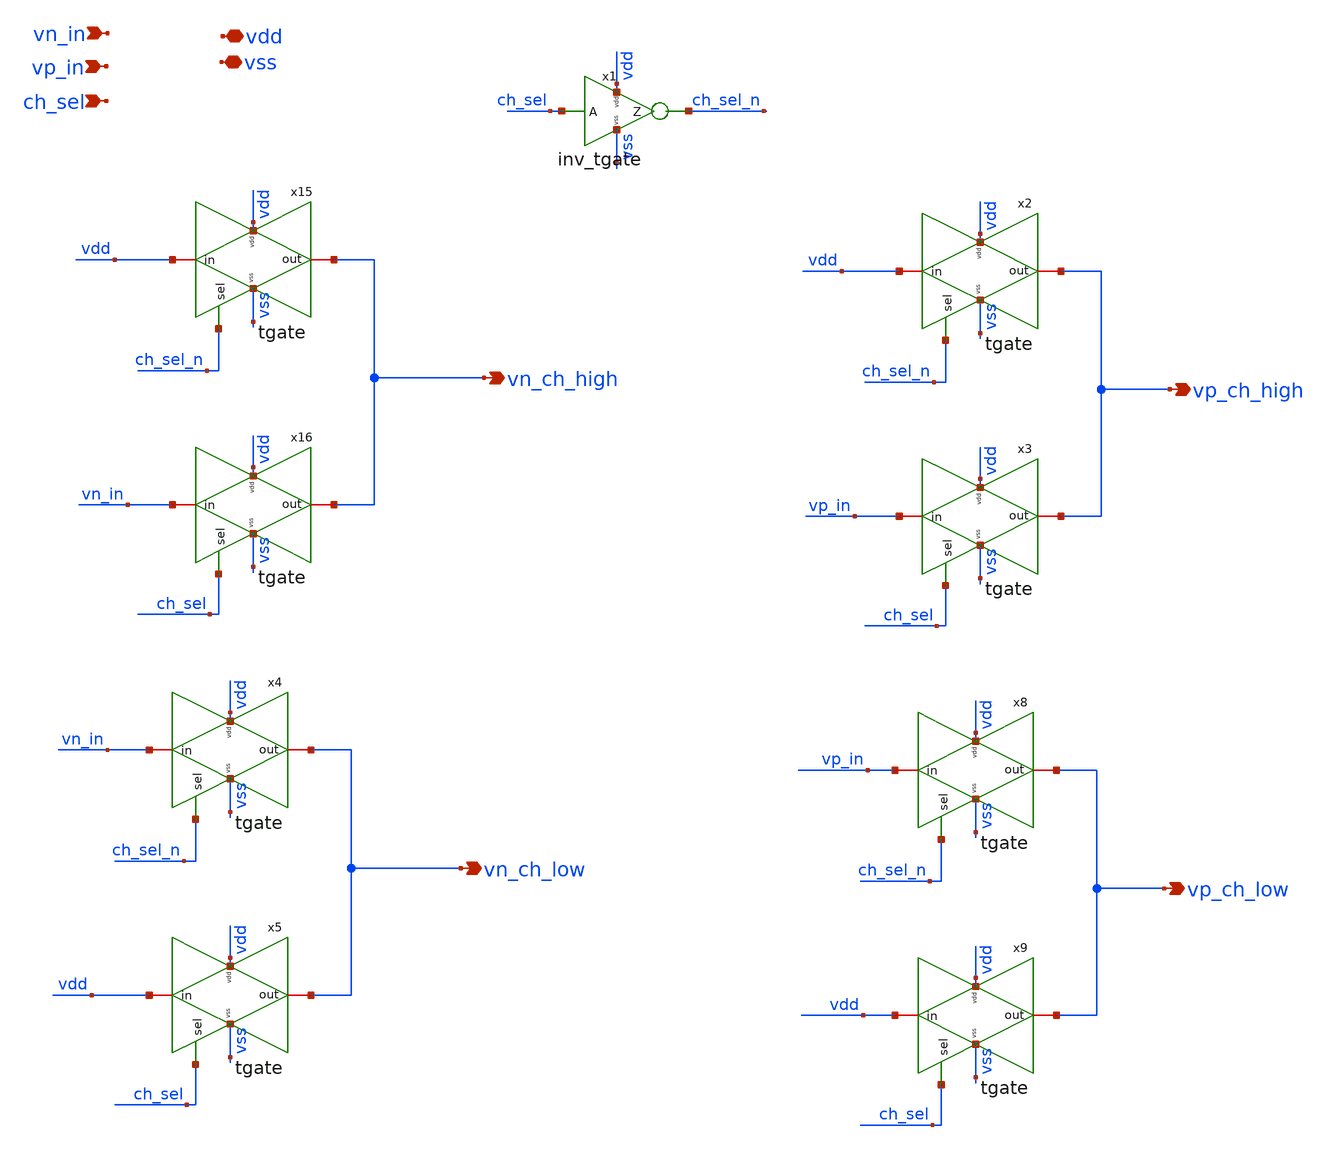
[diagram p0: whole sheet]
** sch_path: v2_feature_extr_withf/vin_sel.sch
**.subckt vin_sel vn_in ch_sel vp_in vdd vss vn_ch_high vp_ch_high vp_ch_low vn_ch_low
*.ipin vn_in
*.ipin ch_sel
*.ipin vp_in
*.iopin vdd
*.iopin vss
*.opin vn_ch_high
*.opin vp_ch_high
*.opin vp_ch_low
*.opin vn_ch_low
x15 vss vdd vdd vn_ch_high ch_sel_n tgate
x16 vss vdd vn_in vn_ch_high ch_sel tgate
x1 vdd ch_sel ch_sel_n vss inv_tgate
x2 vss vdd vdd vp_ch_high ch_sel_n tgate
x3 vss vdd vp_in vp_ch_high ch_sel tgate
x8 vss vdd vp_in vp_ch_low ch_sel_n tgate
x9 vss vdd vdd vp_ch_low ch_sel tgate
x4 vss vdd vn_in vn_ch_low ch_sel_n tgate
x5 vss vdd vdd vn_ch_low ch_sel tgate
**.ends
.end
